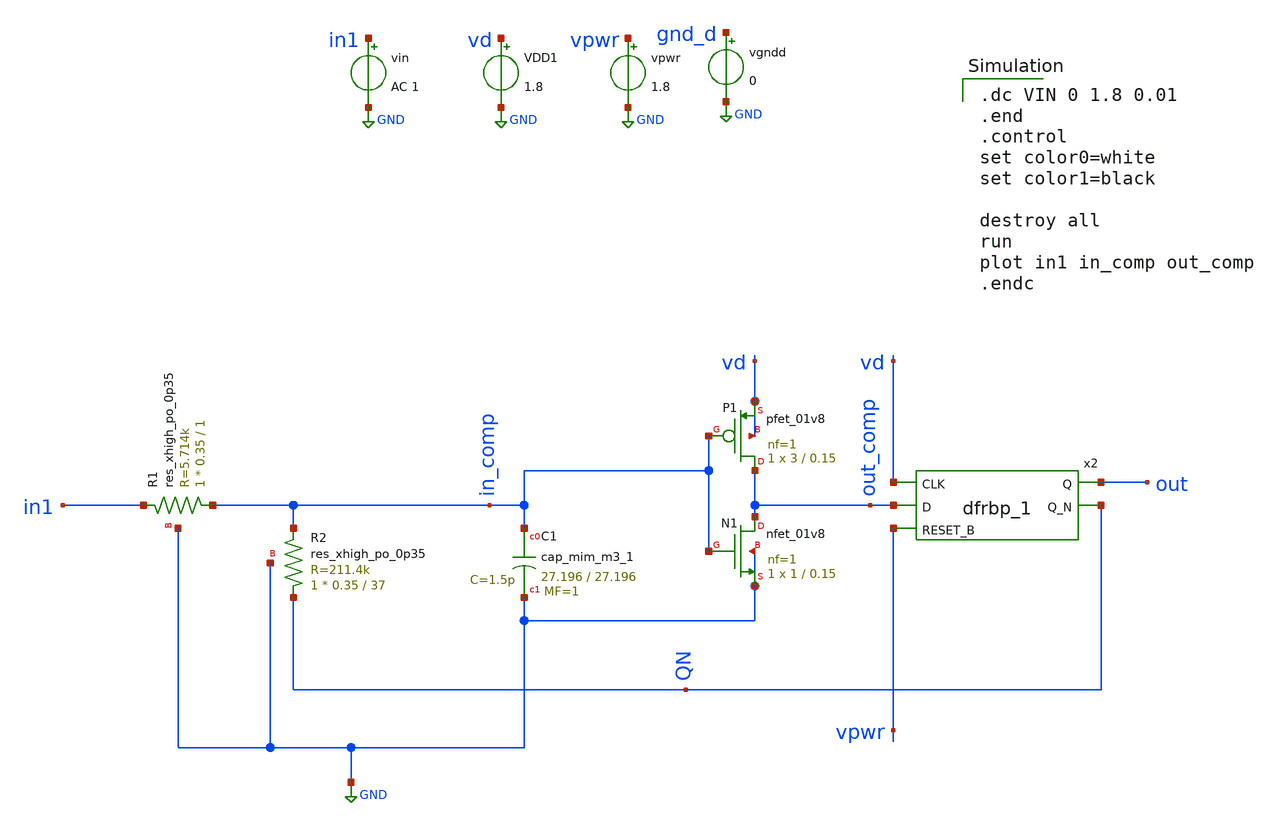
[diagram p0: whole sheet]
** sch_path: mag/sigma-delta_modulator/xschem/comp_tb-dc.sch
* Copyright 2020 Stefan Frederik Schippers
* Licensed under the Apache License, Version 2.0 (the "License");
* you may not use this file except in compliance with the License.
* You may obtain a copy of the License at
* https://www.apache.org/licenses/LICENSE-2.0
* Unless required by applicable law or agreed to in writing, software
* distributed under the License is distributed on an "AS IS" BASIS,
* WITHOUT WARRANTIES OR CONDITIONS OF ANY KIND, either express or implied.
* See the License for the specific language governing permissions and
* limitations under the License.
**.subckt comp_tb-dc
XC1 in_comp GND sky130_fd_pr__cap_mim_m3_1 W=27.196 L=27.196 MF=1 m=1
XR2 QN in_comp GND sky130_fd_pr__res_xhigh_po_0p35 L=37 mult=1 m=1
x2 vd out_comp vpwr gnd_d gnd_d vpwr vpwr out QN sky130_fd_sc_hd__dfrbp_1
XP1 out_comp in_comp vd vd sky130_fd_pr__pfet_01v8 L=0.15 W=3 nf=1 ad='int((nf+1)/2) * W/nf * 0.29' as='int((nf+2)/2) * W/nf * 0.29'
+ pd='2*int((nf+1)/2) * (W/nf + 0.29)' ps='2*int((nf+2)/2) * (W/nf + 0.29)' nrd='0.29 / W' nrs='0.29 / W'
+ sa=0 sb=0 sd=0 mult=1 m=1
XN1 out_comp in_comp GND GND sky130_fd_pr__nfet_01v8 L=0.15 W=1 nf=1 ad='int((nf+1)/2) * W/nf * 0.29'
+ as='int((nf+2)/2) * W/nf * 0.29' pd='2*int((nf+1)/2) * (W/nf + 0.29)' ps='2*int((nf+2)/2) * (W/nf + 0.29)'
+ nrd='0.29 / W' nrs='0.29 / W' sa=0 sb=0 sd=0 mult=1 m=1
XR1 in_comp in1 GND sky130_fd_pr__res_xhigh_po_0p35 L=1 mult=1 m=1
vin in1 GND AC 1
VDD1 vd GND 1.8
vpwr vpwr GND 1.8
vgndd gnd_d GND 0
**** begin user architecture code

.dc VIN 0 1.8 0.01
.end
.control
set color0=white
set color1=black

destroy all
run
plot in1 in_comp out_comp
.endc

 .lib $::SKYWATER_MODELS/sky130.lib.spice tt
.include $::SKYWATER_STDCELLS/sky130_fd_sc_hd.spice

**** end user architecture code
**.ends
.GLOBAL GND
.end
